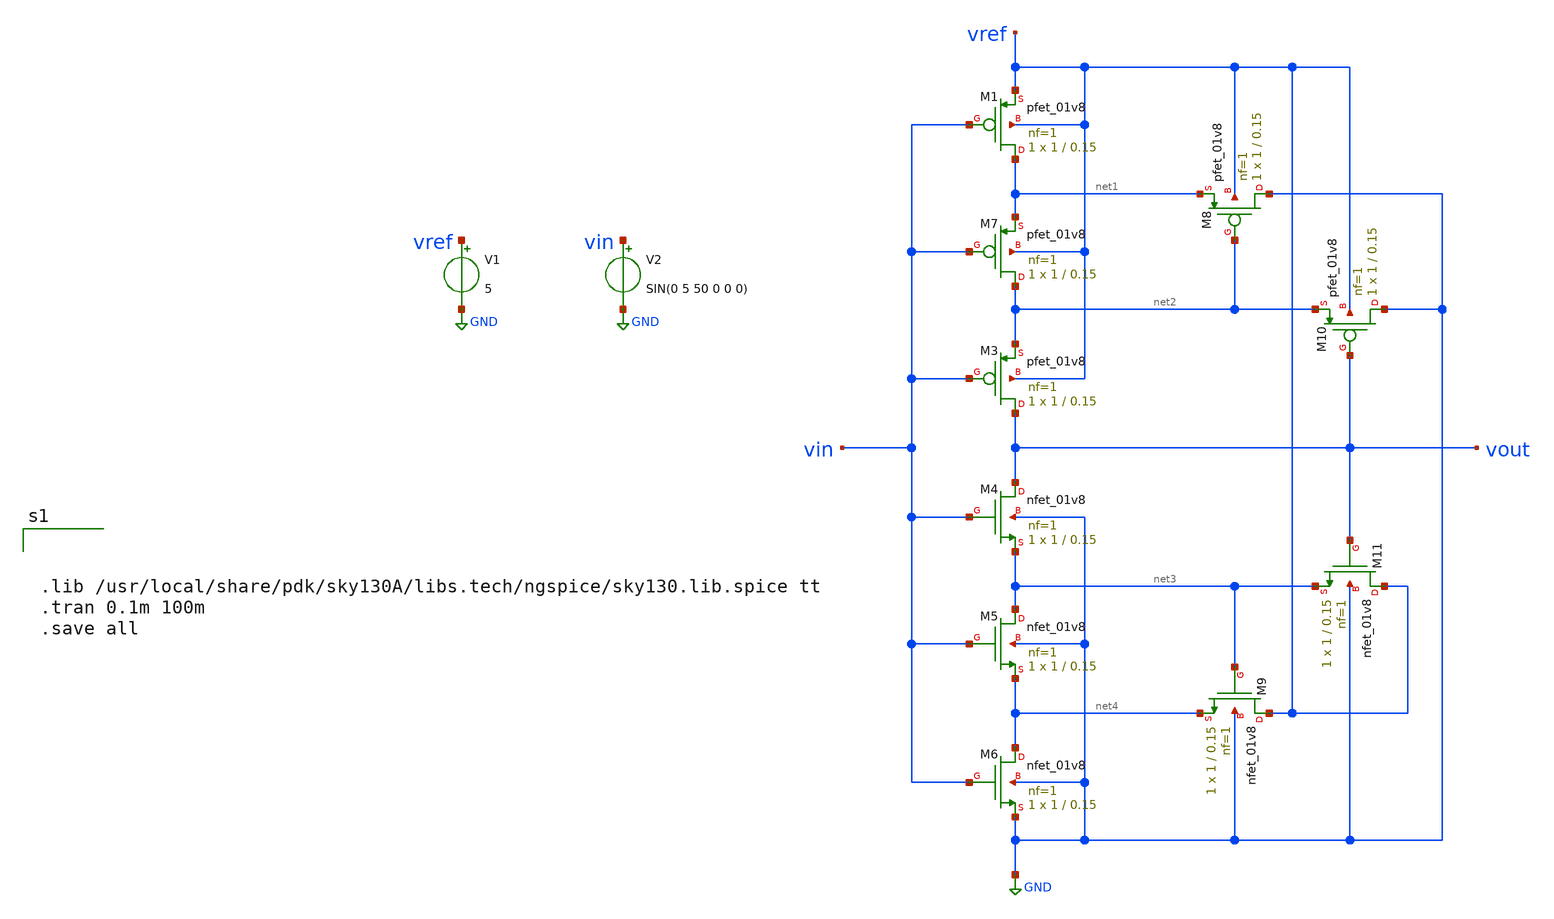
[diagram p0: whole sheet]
** sch_path: Simulation files/schmitt_trigger.sch.sch
**.subckt schmitt_trigger.sch
XM1 net1 vin vref vref sky130_fd_pr__pfet_01v8 L=0.15 W=1 nf=1 ad='int((1 + 1)/2) * 1 / 1 * 0.29' as='int((1 + 2)/2) * 1 / 1 * 0.29'
+ pd='2*int((1 + 1)/2) * (1 / 1 + 0.29)' ps='2*int((1 + 2)/2) * (1 / 1 + 0.29)' nrd='0.29 / 1 ' nrs='0.29 / 1 '
+ sa=0 sb=0 sd=0 mult=1 m=1
XM3 vout vin net2 vref sky130_fd_pr__pfet_01v8 L=0.15 W=1 nf=1 ad='int((1 + 1)/2) * 1 / 1 * 0.29' as='int((1 + 2)/2) * 1 / 1 * 0.29'
+ pd='2*int((1 + 1)/2) * (1 / 1 + 0.29)' ps='2*int((1 + 2)/2) * (1 / 1 + 0.29)' nrd='0.29 / 1 ' nrs='0.29 / 1 '
+ sa=0 sb=0 sd=0 mult=1 m=1
XM4 vout vin net3 GND sky130_fd_pr__nfet_01v8 L=0.15 W=1 nf=1 ad='int((1 + 1)/2) * 1 / 1 * 0.29' as='int((1 + 2)/2) * 1 / 1 * 0.29'
+ pd='2*int((1 + 1)/2) * (1 / 1 + 0.29)' ps='2*int((1 + 2)/2) * (1 / 1 + 0.29)' nrd='0.29 / 1 ' nrs='0.29 / 1 '
+ sa=0 sb=0 sd=0 mult=1 m=1
XM5 net3 vin net4 GND sky130_fd_pr__nfet_01v8 L=0.15 W=1 nf=1 ad='int((1 + 1)/2) * 1 / 1 * 0.29' as='int((1 + 2)/2) * 1 / 1 * 0.29'
+ pd='2*int((1 + 1)/2) * (1 / 1 + 0.29)' ps='2*int((1 + 2)/2) * (1 / 1 + 0.29)' nrd='0.29 / 1 ' nrs='0.29 / 1 '
+ sa=0 sb=0 sd=0 mult=1 m=1
XM6 net4 vin GND GND sky130_fd_pr__nfet_01v8 L=0.15 W=1 nf=1 ad='int((1 + 1)/2) * 1 / 1 * 0.29' as='int((1 + 2)/2) * 1 / 1 * 0.29'
+ pd='2*int((1 + 1)/2) * (1 / 1 + 0.29)' ps='2*int((1 + 2)/2) * (1 / 1 + 0.29)' nrd='0.29 / 1 ' nrs='0.29 / 1 '
+ sa=0 sb=0 sd=0 mult=1 m=1
XM7 net2 vin net1 vref sky130_fd_pr__pfet_01v8 L=0.15 W=1 nf=1 ad='int((1 + 1)/2) * 1 / 1 * 0.29' as='int((1 + 2)/2) * 1 / 1 * 0.29'
+ pd='2*int((1 + 1)/2) * (1 / 1 + 0.29)' ps='2*int((1 + 2)/2) * (1 / 1 + 0.29)' nrd='0.29 / 1 ' nrs='0.29 / 1 '
+ sa=0 sb=0 sd=0 mult=1 m=1
XM8 GND net2 net1 vref sky130_fd_pr__pfet_01v8 L=0.15 W=1 nf=1 ad='int((1 + 1)/2) * 1 / 1 * 0.29' as='int((1 + 2)/2) * 1 / 1 * 0.29'
+ pd='2*int((1 + 1)/2) * (1 / 1 + 0.29)' ps='2*int((1 + 2)/2) * (1 / 1 + 0.29)' nrd='0.29 / 1 ' nrs='0.29 / 1 '
+ sa=0 sb=0 sd=0 mult=1 m=1
XM9 vref net3 net4 GND sky130_fd_pr__nfet_01v8 L=0.15 W=1 nf=1 ad='int((1 + 1)/2) * 1 / 1 * 0.29' as='int((1 + 2)/2) * 1 / 1 * 0.29'
+ pd='2*int((1 + 1)/2) * (1 / 1 + 0.29)' ps='2*int((1 + 2)/2) * (1 / 1 + 0.29)' nrd='0.29 / 1 ' nrs='0.29 / 1 '
+ sa=0 sb=0 sd=0 mult=1 m=1
XM10 GND vout net2 vref sky130_fd_pr__pfet_01v8 L=0.15 W=1 nf=1 ad='int((1 + 1)/2) * 1 / 1 * 0.29' as='int((1 + 2)/2) * 1 / 1 * 0.29'
+ pd='2*int((1 + 1)/2) * (1 / 1 + 0.29)' ps='2*int((1 + 2)/2) * (1 / 1 + 0.29)' nrd='0.29 / 1 ' nrs='0.29 / 1 '
+ sa=0 sb=0 sd=0 mult=1 m=1
XM11 vref vout net3 GND sky130_fd_pr__nfet_01v8 L=0.15 W=1 nf=1 ad='int((1 + 1)/2) * 1 / 1 * 0.29' as='int((1 + 2)/2) * 1 / 1 * 0.29'
+ pd='2*int((1 + 1)/2) * (1 / 1 + 0.29)' ps='2*int((1 + 2)/2) * (1 / 1 + 0.29)' nrd='0.29 / 1 ' nrs='0.29 / 1 '
+ sa=0 sb=0 sd=0 mult=1 m=1
V1 vref GND 5
V2 vin GND SIN(0 5 50 0 0 0)
**** begin user architecture code



.lib /usr/local/share/pdk/sky130A/libs.tech/ngspice/sky130.lib.spice tt
.tran 0.1m 100m
.save all



**** end user architecture code
**.ends
.GLOBAL GND
.end
